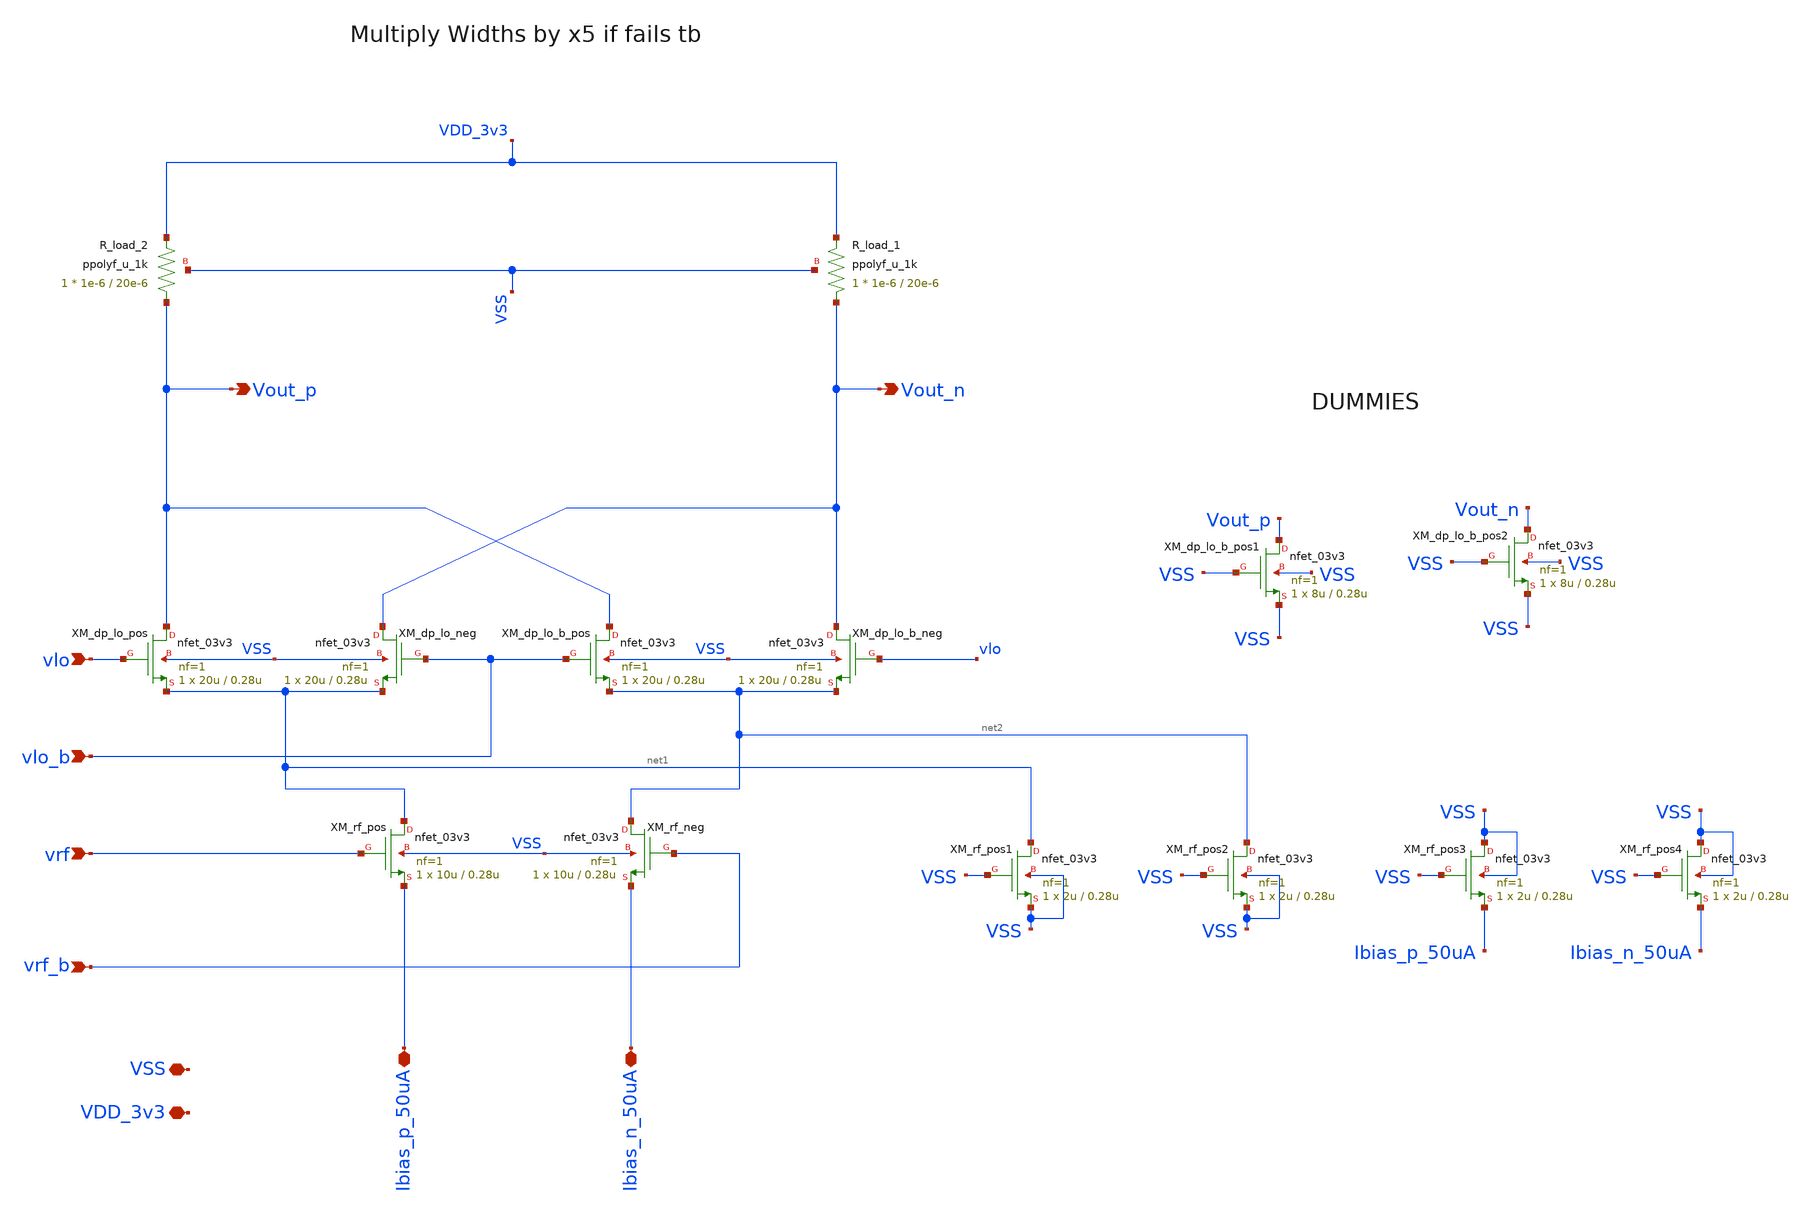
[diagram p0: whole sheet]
** sch_path: Analog/schematics/2_mixer/gilbert_mixer.sch
**.subckt gilbert_mixer vlo vlo_b vrf vrf_b Vout_p Vout_n Ibias_n_50uA Ibias_p_50uA VSS VDD_3v3
*.ipin vlo
*.ipin vlo_b
*.ipin vrf
*.ipin vrf_b
*.opin Vout_p
*.opin Vout_n
*.iopin Ibias_n_50uA
*.iopin Ibias_p_50uA
*.iopin VSS
*.iopin VDD_3v3
XM_dp_lo_pos Vout_p vlo net1 VSS nfet_03v3 L=0.28u W=20u nf=1 ad='int((nf+1)/2) * W/nf * 0.18u' as='int((nf+2)/2) * W/nf * 0.18u'
+ pd='2*int((nf+1)/2) * (W/nf + 0.18u)' ps='2*int((nf+2)/2) * (W/nf + 0.18u)' nrd='0.18u / W' nrs='0.18u / W'
+ sa=0 sb=0 sd=0 m=1
XM_dp_lo_neg Vout_n vlo_b net1 VSS nfet_03v3 L=0.28u W=20u nf=1 ad='int((nf+1)/2) * W/nf * 0.18u' as='int((nf+2)/2) * W/nf * 0.18u'
+ pd='2*int((nf+1)/2) * (W/nf + 0.18u)' ps='2*int((nf+2)/2) * (W/nf + 0.18u)' nrd='0.18u / W' nrs='0.18u / W'
+ sa=0 sb=0 sd=0 m=1
XM_dp_lo_b_pos Vout_p vlo_b net2 VSS nfet_03v3 L=0.28u W=20u nf=1 ad='int((nf+1)/2) * W/nf * 0.18u' as='int((nf+2)/2) * W/nf * 0.18u'
+ pd='2*int((nf+1)/2) * (W/nf + 0.18u)' ps='2*int((nf+2)/2) * (W/nf + 0.18u)' nrd='0.18u / W' nrs='0.18u / W'
+ sa=0 sb=0 sd=0 m=1
XM_dp_lo_b_neg Vout_n vlo net2 VSS nfet_03v3 L=0.28u W=20u nf=1 ad='int((nf+1)/2) * W/nf * 0.18u' as='int((nf+2)/2) * W/nf * 0.18u'
+ pd='2*int((nf+1)/2) * (W/nf + 0.18u)' ps='2*int((nf+2)/2) * (W/nf + 0.18u)' nrd='0.18u / W' nrs='0.18u / W'
+ sa=0 sb=0 sd=0 m=1
XM_rf_pos net1 vrf Ibias_p_50uA VSS nfet_03v3 L=0.28u W=10u nf=1 ad='int((nf+1)/2) * W/nf * 0.18u' as='int((nf+2)/2) * W/nf * 0.18u'
+ pd='2*int((nf+1)/2) * (W/nf + 0.18u)' ps='2*int((nf+2)/2) * (W/nf + 0.18u)' nrd='0.18u / W' nrs='0.18u / W'
+ sa=0 sb=0 sd=0 m=1
XM_rf_neg net2 vrf_b Ibias_n_50uA VSS nfet_03v3 L=0.28u W=10u nf=1 ad='int((nf+1)/2) * W/nf * 0.18u'
+ as='int((nf+2)/2) * W/nf * 0.18u' pd='2*int((nf+1)/2) * (W/nf + 0.18u)' ps='2*int((nf+2)/2) * (W/nf + 0.18u)'
+ nrd='0.18u / W' nrs='0.18u / W' sa=0 sb=0 sd=0 m=1
XR_load_2 Vout_p VDD_3v3 VSS ppolyf_u_1k r_width=1e-6 r_length=20e-6 m=1
XR_load_1 Vout_n VDD_3v3 VSS ppolyf_u_1k r_width=1e-6 r_length=20e-6 m=1
XM_rf_pos1 net1 VSS VSS VSS nfet_03v3 L=0.28u W=2u nf=1 ad='int((nf+1)/2) * W/nf * 0.18u' as='int((nf+2)/2) * W/nf * 0.18u'
+ pd='2*int((nf+1)/2) * (W/nf + 0.18u)' ps='2*int((nf+2)/2) * (W/nf + 0.18u)' nrd='0.18u / W' nrs='0.18u / W'
+ sa=0 sb=0 sd=0 m=1
XM_dp_lo_b_pos1 Vout_p VSS VSS VSS nfet_03v3 L=0.28u W=8u nf=1 ad='int((nf+1)/2) * W/nf * 0.18u' as='int((nf+2)/2) * W/nf * 0.18u'
+ pd='2*int((nf+1)/2) * (W/nf + 0.18u)' ps='2*int((nf+2)/2) * (W/nf + 0.18u)' nrd='0.18u / W' nrs='0.18u / W'
+ sa=0 sb=0 sd=0 m=1
XM_dp_lo_b_pos2 Vout_n VSS VSS VSS nfet_03v3 L=0.28u W=8u nf=1 ad='int((nf+1)/2) * W/nf * 0.18u' as='int((nf+2)/2) * W/nf * 0.18u'
+ pd='2*int((nf+1)/2) * (W/nf + 0.18u)' ps='2*int((nf+2)/2) * (W/nf + 0.18u)' nrd='0.18u / W' nrs='0.18u / W'
+ sa=0 sb=0 sd=0 m=1
XM_rf_pos2 net2 VSS VSS VSS nfet_03v3 L=0.28u W=2u nf=1 ad='int((nf+1)/2) * W/nf * 0.18u' as='int((nf+2)/2) * W/nf * 0.18u'
+ pd='2*int((nf+1)/2) * (W/nf + 0.18u)' ps='2*int((nf+2)/2) * (W/nf + 0.18u)' nrd='0.18u / W' nrs='0.18u / W'
+ sa=0 sb=0 sd=0 m=1
XM_rf_pos3 VSS VSS Ibias_p_50uA VSS nfet_03v3 L=0.28u W=2u nf=1 ad='int((nf+1)/2) * W/nf * 0.18u' as='int((nf+2)/2) * W/nf * 0.18u'
+ pd='2*int((nf+1)/2) * (W/nf + 0.18u)' ps='2*int((nf+2)/2) * (W/nf + 0.18u)' nrd='0.18u / W' nrs='0.18u / W'
+ sa=0 sb=0 sd=0 m=1
XM_rf_pos4 VSS VSS Ibias_n_50uA VSS nfet_03v3 L=0.28u W=2u nf=1 ad='int((nf+1)/2) * W/nf * 0.18u' as='int((nf+2)/2) * W/nf * 0.18u'
+ pd='2*int((nf+1)/2) * (W/nf + 0.18u)' ps='2*int((nf+2)/2) * (W/nf + 0.18u)' nrd='0.18u / W' nrs='0.18u / W'
+ sa=0 sb=0 sd=0 m=1
**.ends
.end
